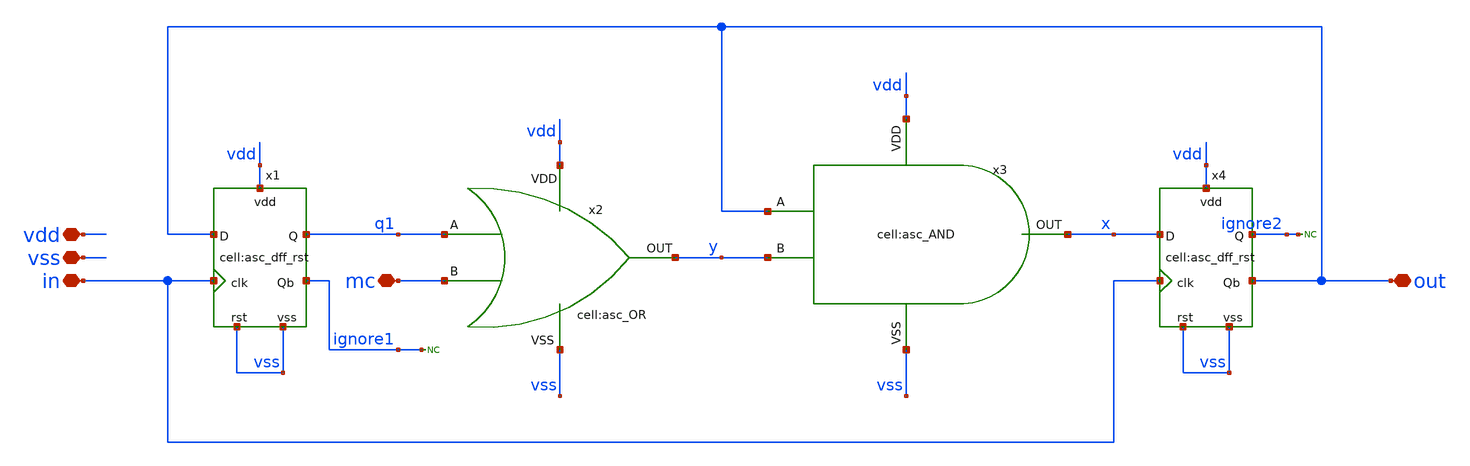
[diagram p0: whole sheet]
** sch_path: designs/libs/core_analog/asc_dual_mod_pre_2_3_20250809/asc_dual_mod_pre_2_3_20250809.sch
**.subckt asc_dual_mod_pre_2_3_20250809 vdd vss in mc out
*.iopin vdd
*.iopin vss
*.iopin in
*.iopin mc
*.iopin out
x2 vdd vss y q1 mc asc_OR
x3 vdd x out y vss asc_AND
* noconn ignore1
* noconn ignore2
x1 in out ignore1 vdd vss q1 vss asc_dff_rst
x4 in x out vdd vss ignore2 vss asc_dff_rst
**.ends
.end
